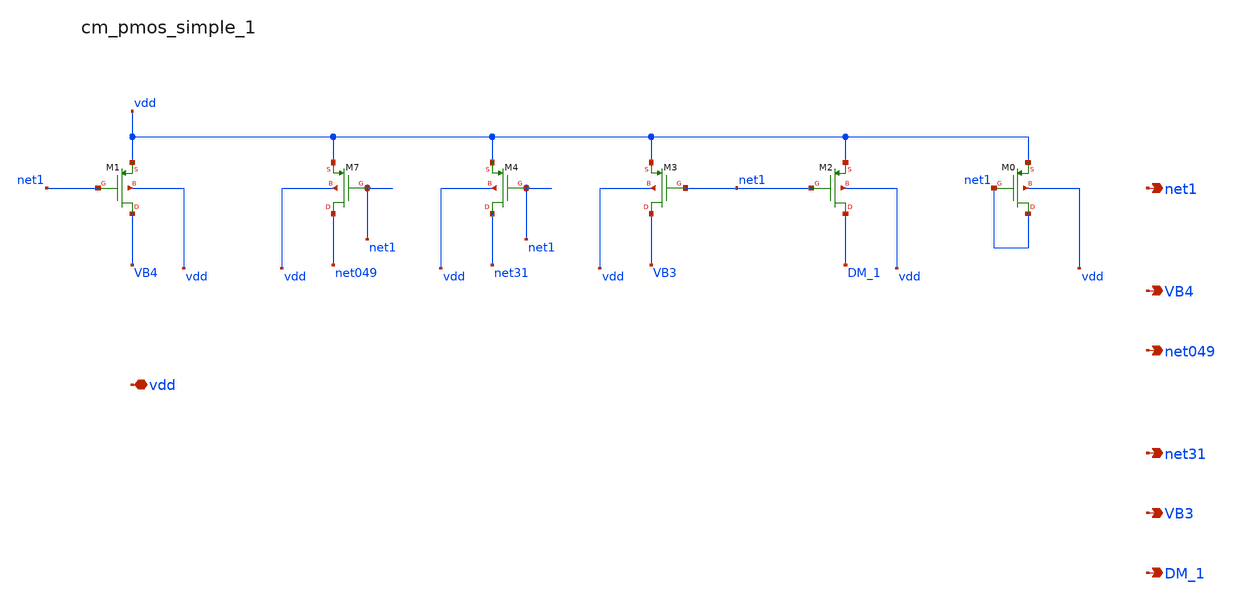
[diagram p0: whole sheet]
** sch_path: analog-db/raw/amp_007_leung_dfcfc2/hier/blocks/cm_pmos_simple_1.sch
**.subckt cm_pmos_simple_1 vdd net1 VB4 net049 net31 VB3 DM_1
*.iopin vdd
*.opin net1
*.opin VB4
*.opin net049
*.opin net31
*.opin VB3
*.opin DM_1
XM0 net1 net1 vdd vdd sg13_lv_pmos w=x_dut_xm0_w l=x_dut_xm0_l ng=1 m=x_dut_xm0_m
XM1 VB4 net1 vdd vdd sg13_lv_pmos w=x_dut_xm1_w l=x_dut_xm1_l ng=1 m=x_dut_xm1_m
XM2 DM_1 net1 vdd vdd sg13_lv_pmos w=x_dut_xm2_w l=x_dut_xm2_l ng=1 m=x_dut_xm2_m
XM3 VB3 net1 vdd vdd sg13_lv_pmos w=x_dut_xm3_w l=x_dut_xm3_l ng=1 m=x_dut_xm3_m
XM4 net31 net1 vdd vdd sg13_lv_pmos w=x_dut_xm4_w l=x_dut_xm4_l ng=1 m=x_dut_xm4_m
XM7 net049 net1 vdd vdd sg13_lv_pmos w=x_dut_xm7_w l=x_dut_xm7_l ng=1 m=x_dut_xm7_m
**.ends
.end
